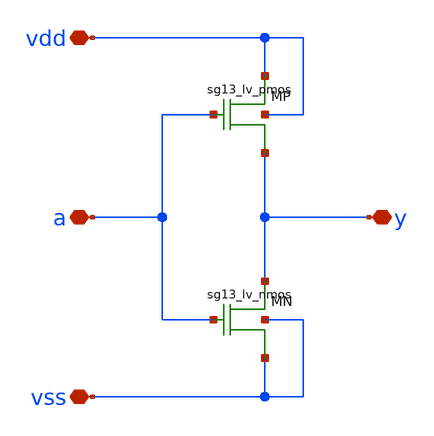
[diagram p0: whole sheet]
** sch_path: xschem/logic_gates/INVLV.sch
**.subckt INVLV vdd vss y a
*.iopin vdd
*.iopin vss
*.iopin y
*.iopin a
XMP vdd a y vdd sg13_lv_pmos w=1.0u l=0.13u ng=1 m=1
XMN y a vss vss sg13_lv_nmos w=0.5u l=0.13u ng=1 m=1
**.ends
.end
